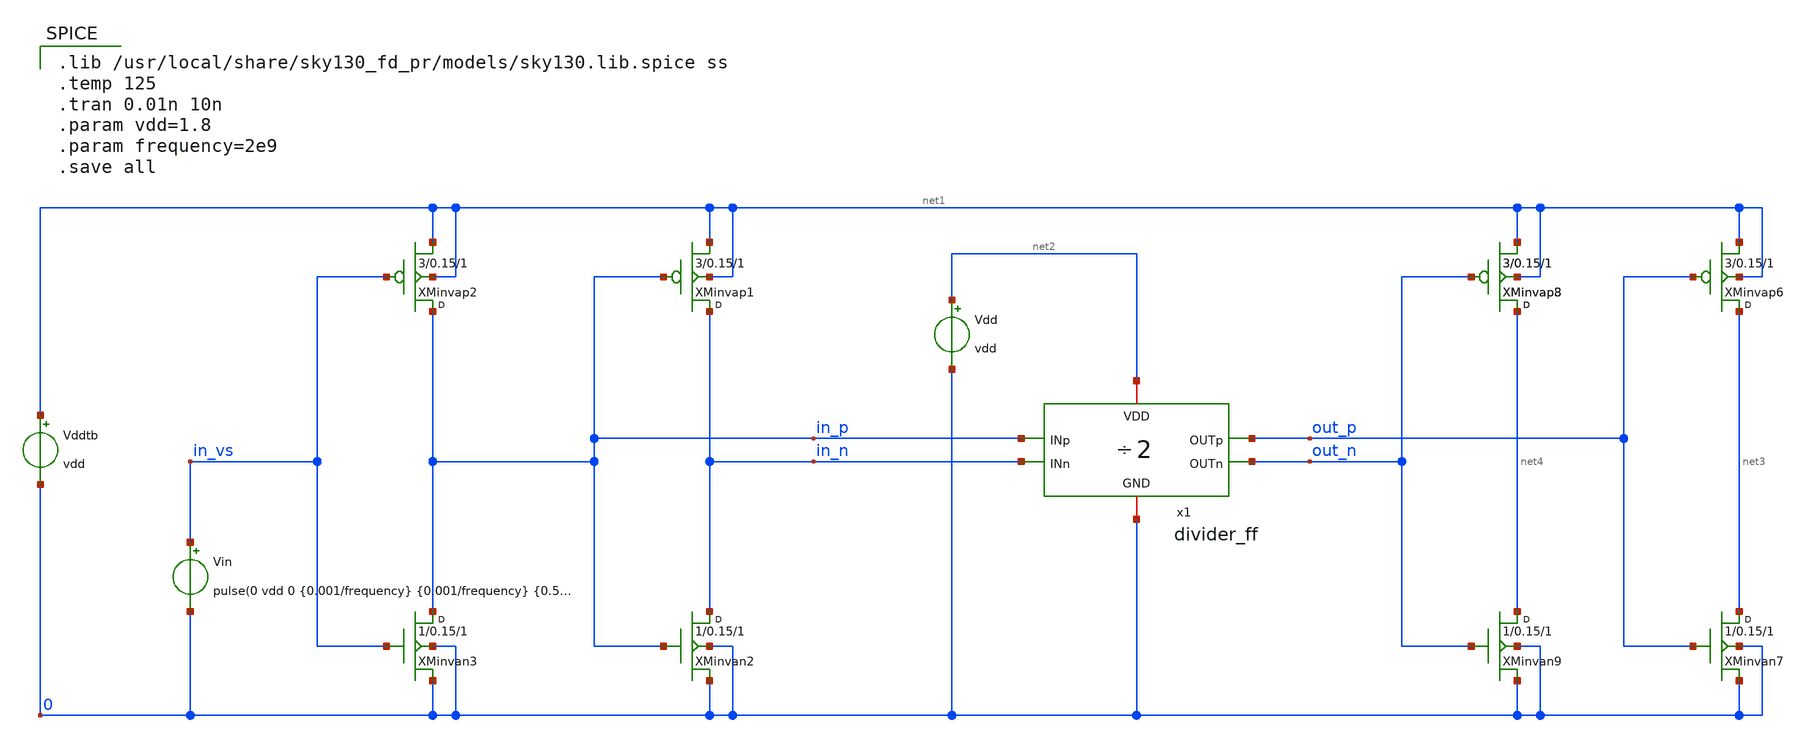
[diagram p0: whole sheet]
** sch_path: design/divider_ff/test/divider_ff_test.sch
**.subckt divider_ff_test
XMinvap1 in_n in_p net1 net1 sky130_fd_pr__pfet_01v8 w=3 l=0.15 m=1
XMinvan2 in_n in_p 0 0 sky130_fd_pr__nfet_01v8 w=1 l=0.15 m=1
Vin in_vs 0 pulse(0 vdd 0 {0.001/frequency} {0.001/frequency} {0.5/frequency} {1.0/frequency} 0)
XMinvap2 in_p in_vs net1 net1 sky130_fd_pr__pfet_01v8 w=3 l=0.15 m=1
XMinvan3 in_p in_vs 0 0 sky130_fd_pr__nfet_01v8 w=1 l=0.15 m=1
XMinvap3 net4 out_n net1 net1 sky130_fd_pr__pfet_01v8 w=3 l=0.15 m=1
XMinvap6 net3 out_p net1 net1 sky130_fd_pr__pfet_01v8 w=3 l=0.15 m=1
XMinvan7 net3 out_p 0 0 sky130_fd_pr__nfet_01v8 w=1 l=0.15 m=1
XMinvap8 net4 out_n net1 net1 sky130_fd_pr__pfet_01v8 w=3 l=0.15 m=1
XMinvan9 net4 out_n 0 0 sky130_fd_pr__nfet_01v8 w=1 l=0.15 m=1
x1 net2 out_p out_n in_p in_n 0 divider_ff
Vddtb net1 0 vdd
Vdd net2 0 vdd
**** begin user architecture code

.lib /usr/local/share/sky130_fd_pr/models/sky130.lib.spice ss
.temp 125
.tran 0.01n 10n
.param vdd=1.8
.param frequency=2e9
.save all

**** end user architecture code
**.ends

* expanding   symbol:  divider_ff/divider_ff.sym # of pins=6
** sym_path: design/divider_ff/divider_ff.sym
** sch_path: design/divider_ff/divider_ff.sch
.subckt divider_ff VDD OUTp OUTn INp INn GND
*.ipin INn
*.opin OUTp
*.iopin VDD
*.iopin GND
*.opin OUTn
*.ipin INp
XMpasspba net2 OUTp VDD VDD sky130_fd_pr__pfet_01v8 L=0.15 W=1.5 nf=1 ad='W * 0.29' as='W * 0.29' pd='W + 2 * 0.29'
+ ps='W + 2 * 0.29' nrd=0 nrs=0 sa=0 sb=0 sd=0 mult=2 m=2
XMpasspca net1 INn net2 VDD sky130_fd_pr__pfet_01v8 L=0.15 W=1.5 nf=1 ad='W * 0.29' as='W * 0.29' pd='W + 2 * 0.29'
+ ps='W + 2 * 0.29' nrd=0 nrs=0 sa=0 sb=0 sd=0 mult=2 m=2
XMpasspba1Minvap net4 net1 VDD VDD sky130_fd_pr__pfet_01v8 L=0.15 W=1.5 nf=1 ad='W * 0.29' as='W * 0.29'
+ pd='W + 2 * 0.29' ps='W + 2 * 0.29' nrd=0 nrs=0 sa=0 sb=0 sd=0 mult=2 m=2
XMpasspba3 net6 net4 VDD VDD sky130_fd_pr__pfet_01v8 L=0.15 W=1.5 nf=1 ad='W * 0.29' as='W * 0.29' pd='W + 2 * 0.29'
+ ps='W + 2 * 0.29' nrd=0 nrs=0 sa=0 sb=0 sd=0 mult=2 m=2
XMpasspca2 net5 INp net6 VDD sky130_fd_pr__pfet_01v8 L=0.15 W=1.5 nf=1 ad='W * 0.29' as='W * 0.29' pd='W + 2 * 0.29'
+ ps='W + 2 * 0.29' nrd=0 nrs=0 sa=0 sb=0 sd=0 mult=2 m=2
XMinvap5 OUTn net5 VDD VDD sky130_fd_pr__pfet_01v8 L=0.15 W=1.5 nf=1 ad='W * 0.29' as='W * 0.29' pd='W + 2 * 0.29'
+ ps='W + 2 * 0.29' nrd=0 nrs=0 sa=0 sb=0 sd=0 mult=2 m=2
XMinvap1 OUTp OUTn VDD VDD sky130_fd_pr__pfet_01v8 L=0.15 W=1.5 nf=1 ad='W * 0.29' as='W * 0.29' pd='W + 2 * 0.29'
+ ps='W + 2 * 0.29' nrd=0 nrs=0 sa=0 sb=0 sd=0 mult=2 m=2
XMpassnca net1 INp net3 GND sky130_fd_pr__nfet_01v8 L=0.15 W=1 nf=1 ad='W * 0.29' as='W * 0.29' pd='W + 2 * 0.29'
+ ps='W + 2 * 0.29' nrd=0 nrs=0 sa=0 sb=0 sd=0 mult=1 m=1
XMpassnba net3 OUTp GND GND sky130_fd_pr__nfet_01v8 L=0.15 W=1 nf=1 ad='W * 0.29' as='W * 0.29' pd='W + 2 * 0.29'
+ ps='W + 2 * 0.29' nrd=0 nrs=0 sa=0 sb=0 sd=0 mult=1 m=1
XMinvan net4 net1 GND GND sky130_fd_pr__nfet_01v8 L=0.15 W=1 nf=1 ad='W * 0.29' as='W * 0.29' pd='W + 2 * 0.29'
+ ps='W + 2 * 0.29' nrd=0 nrs=0 sa=0 sb=0 sd=0 mult=1 m=1
XMpassnca1 net5 INn net7 GND sky130_fd_pr__nfet_01v8 L=0.15 W=1 nf=1 ad='W * 0.29' as='W * 0.29' pd='W + 2 * 0.29'
+ ps='W + 2 * 0.29' nrd=0 nrs=0 sa=0 sb=0 sd=0 mult=1 m=1
XMpassnba4 net7 net4 GND GND sky130_fd_pr__nfet_01v8 L=0.15 W=1 nf=1 ad='W * 0.29' as='W * 0.29' pd='W + 2 * 0.29'
+ ps='W + 2 * 0.29' nrd=0 nrs=0 sa=0 sb=0 sd=0 mult=1 m=1
XMinvan6 OUTn net5 GND GND sky130_fd_pr__nfet_01v8 L=0.15 W=1 nf=1 ad='W * 0.29' as='W * 0.29' pd='W + 2 * 0.29'
+ ps='W + 2 * 0.29' nrd=0 nrs=0 sa=0 sb=0 sd=0 mult=1 m=1
XMinvan2 OUTp OUTn GND GND sky130_fd_pr__nfet_01v8 L=0.15 W=1 nf=1 ad='W * 0.29' as='W * 0.29' pd='W + 2 * 0.29'
+ ps='W + 2 * 0.29' nrd=0 nrs=0 sa=0 sb=0 sd=0 mult=1 m=1
.ends

.end
